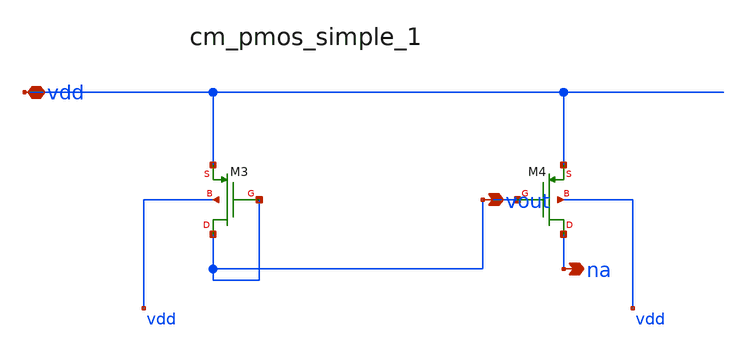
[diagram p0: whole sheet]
** sch_path: analog-db/raw/tsn_003_ptat_4t_xcoupled/hier/blocks/cm_pmos_simple_1.sch
**.subckt cm_pmos_simple_1 vdd vout na
*.iopin vdd
*.opin vout
*.opin na
XM3 vout vout vdd vdd sg13_lv_pmos w=x_dut_xm3_w l=x_dut_xm3_l ng=1 m=x_dut_xm3_m
XM4 na vout vdd vdd sg13_lv_pmos w=x_dut_xm4_w l=x_dut_xm4_l ng=1 m=x_dut_xm4_m
**.ends
.end
